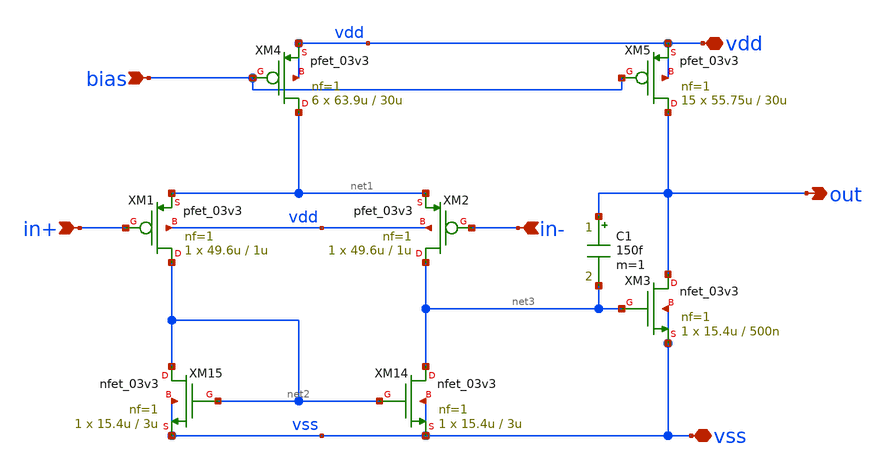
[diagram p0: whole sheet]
** sch_path: design/analog/OTA/two-stage_miller_OTA.sch
**.subckt two-stage_miller_OTA in- in+ out vdd vss bias
*.ipin in-
*.ipin in+
*.opin out
*.iopin vdd
*.iopin vss
*.ipin bias
XM1 net2 in+ net1 vdd pfet_03v3 L=1u W=49.6u nf=1 ad='int((nf+1)/2) * W/nf * 0.18u' as='int((nf+2)/2) * W/nf * 0.18u'
+ pd='2*int((nf+1)/2) * (W/nf + 0.18u)' ps='2*int((nf+2)/2) * (W/nf + 0.18u)' nrd='0.18u / W' nrs='0.18u / W'
+ sa=0 sb=0 sd=0 m=1
XM2 net3 in- net1 vdd pfet_03v3 L=1u W=49.6u nf=1 ad='int((nf+1)/2) * W/nf * 0.18u' as='int((nf+2)/2) * W/nf * 0.18u'
+ pd='2*int((nf+1)/2) * (W/nf + 0.18u)' ps='2*int((nf+2)/2) * (W/nf + 0.18u)' nrd='0.18u / W' nrs='0.18u / W'
+ sa=0 sb=0 sd=0 m=1
XM14 net3 net2 vss vss nfet_03v3 L=3u W=15.4u nf=1 ad='int((nf+1)/2) * W/nf * 0.18u' as='int((nf+2)/2) * W/nf * 0.18u'
+ pd='2*int((nf+1)/2) * (W/nf + 0.18u)' ps='2*int((nf+2)/2) * (W/nf + 0.18u)' nrd='0.18u / W' nrs='0.18u / W'
+ sa=0 sb=0 sd=0 m=1
XM15 net2 net2 vss vss nfet_03v3 L=3u W=15.4u nf=1 ad='int((nf+1)/2) * W/nf * 0.18u' as='int((nf+2)/2) * W/nf * 0.18u'
+ pd='2*int((nf+1)/2) * (W/nf + 0.18u)' ps='2*int((nf+2)/2) * (W/nf + 0.18u)' nrd='0.18u / W' nrs='0.18u / W'
+ sa=0 sb=0 sd=0 m=1
XM3 out net3 vss vss nfet_03v3 L=500n W=15.4u nf=1 ad='int((nf+1)/2) * W/nf * 0.18u' as='int((nf+2)/2) * W/nf * 0.18u'
+ pd='2*int((nf+1)/2) * (W/nf + 0.18u)' ps='2*int((nf+2)/2) * (W/nf + 0.18u)' nrd='0.18u / W' nrs='0.18u / W'
+ sa=0 sb=0 sd=0 m=1
C1 out net3 150f m=1
XM4 net1 bias vdd vdd pfet_03v3 L=30u W=63.9u nf=1 ad='int((nf+1)/2) * W/nf * 0.18u' as='int((nf+2)/2) * W/nf * 0.18u'
+ pd='2*int((nf+1)/2) * (W/nf + 0.18u)' ps='2*int((nf+2)/2) * (W/nf + 0.18u)' nrd='0.18u / W' nrs='0.18u / W'
+ sa=0 sb=0 sd=0 m=6
XM5 out bias vdd vdd pfet_03v3 L=30u W=55.75u nf=1 ad='int((nf+1)/2) * W/nf * 0.18u' as='int((nf+2)/2) * W/nf * 0.18u'
+ pd='2*int((nf+1)/2) * (W/nf + 0.18u)' ps='2*int((nf+2)/2) * (W/nf + 0.18u)' nrd='0.18u / W' nrs='0.18u / W'
+ sa=0 sb=0 sd=0 m=15
**.ends
.end
